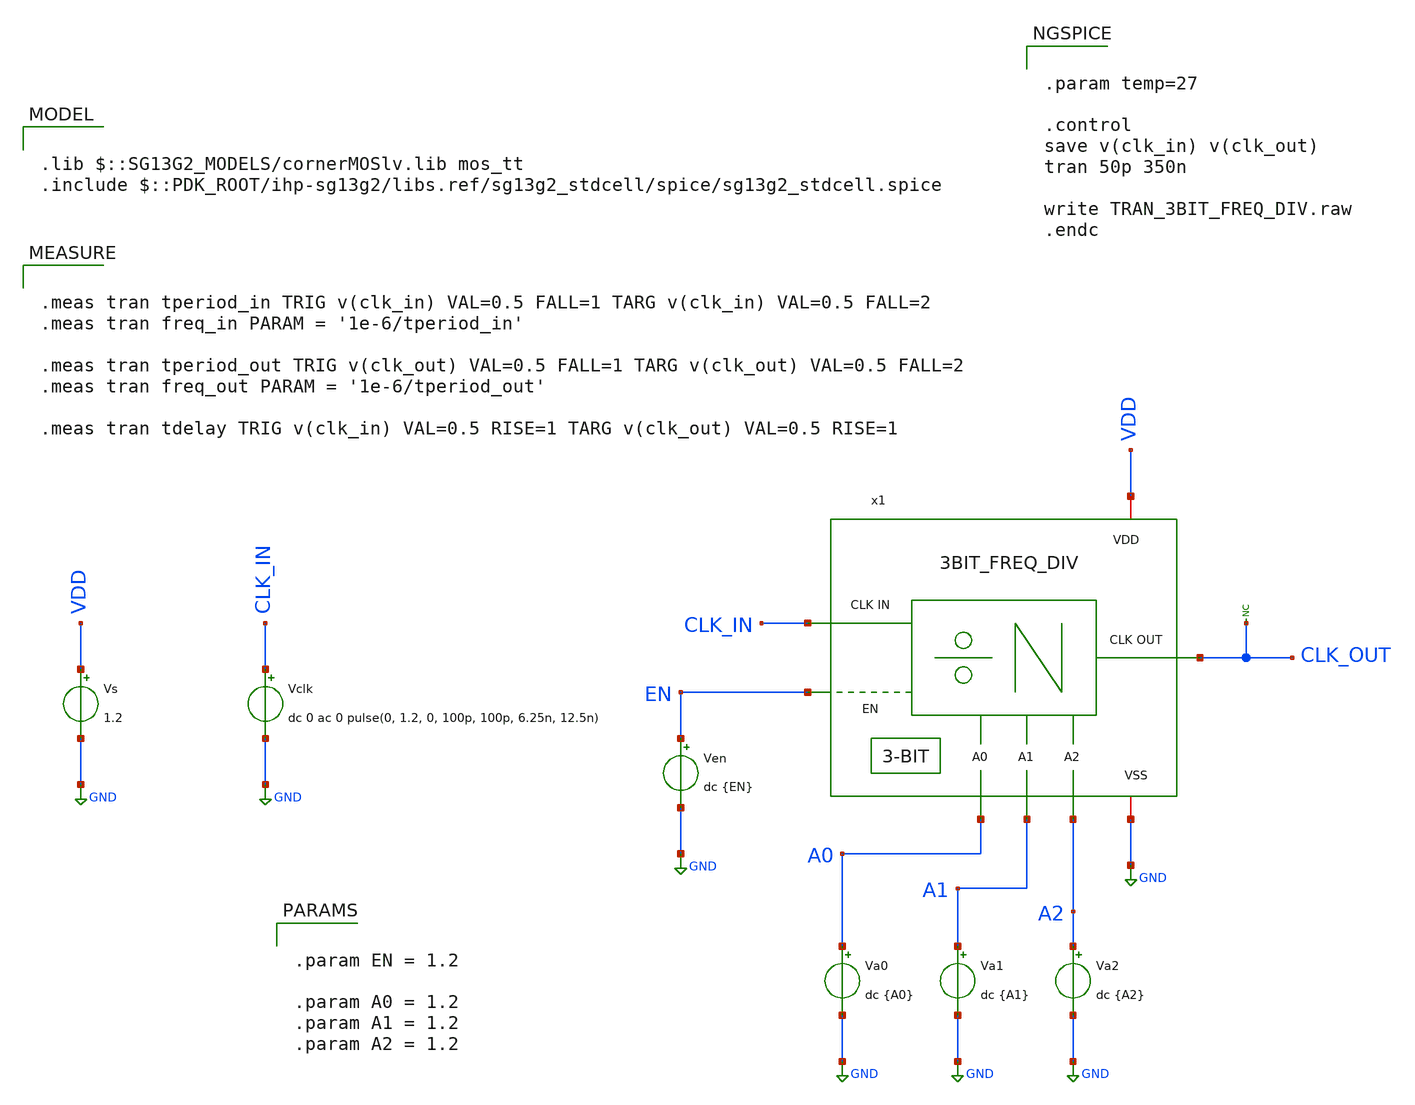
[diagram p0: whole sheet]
** sch_path: 30_MHz_Fractional_N_PLL/design_data/xschem/3BIT_FREQ_DIV_TB.sch
* IHP-GmbH/IHP-Open-PDK/ihp-sg13g2/libs.tech/xschem/sg13g2_stdcells/sg13g2_or3_1.sch:
* Copyright 2023 IHP PDK Authors
* Licensed under the Apache License, Version 2.0 (the "License");

.lib $::SG13G2_MODELS/cornerMOSlv.lib mos_tt
.include $::PDK_ROOT/ihp-sg13g2/libs.ref/sg13g2_stdcell/spice/sg13g2_stdcell.spice

**.subckt 3BIT_FREQ_DIV_TB
Vs VDD GND 1.2
Vclk CLK_IN GND dc 0 ac 0 pulse(0, 1.2, 0, 100p, 100p, 6.25n, 12.5n)
* noconn CLK_OUT
Ven EN GND dc {EN}
Va1 A1 GND dc {A1}
Va2 A2 GND dc {A2}
x1 A0 CLK_IN EN CLK_OUT A1 VDD GND A2 3BIT_FREQ_DIV
Va0 A0 GND dc {A0}
**** begin user architecture code


.meas tran tperiod_in TRIG v(clk_in) VAL=0.5 FALL=1 TARG v(clk_in) VAL=0.5 FALL=2
.meas tran freq_in PARAM = '1e-6/tperiod_in'

.meas tran tperiod_out TRIG v(clk_out) VAL=0.5 FALL=1 TARG v(clk_out) VAL=0.5 FALL=2
.meas tran freq_out PARAM = '1e-6/tperiod_out'

.meas tran tdelay TRIG v(clk_in) VAL=0.5 RISE=1 TARG v(clk_out) VAL=0.5 RISE=1




.param EN = 1.2

.param A0 = 1.2
.param A1 = 1.2
.param A2 = 1.2




.param temp=27

.control
save v(clk_in) v(clk_out)
tran 50p 350n

write TRAN_3BIT_FREQ_DIV.raw
.endc


**** end user architecture code
**.ends

* expanding   symbol:  3BIT_FREQ_DIV.sym # of pins=8
** sym_path: 30_MHz_Fractional_N_PLL/design_data/xschem/3BIT_FREQ_DIV.sym
** sch_path: 30_MHz_Fractional_N_PLL/design_data/xschem/3BIT_FREQ_DIV.sch
.subckt 3BIT_FREQ_DIV A0 CLK_IN EN CLK_OUT A1 VDD VSS A2
*.ipin CLK_IN
*.ipin EN
*.ipin A0
*.ipin A1
*.opin CLK_OUT
*.iopin VSS
*.iopin VDD
*.ipin A2
x1 VDD VSS nEQ0 net1 CLK net2 DIV_RST A0 FREQ_DIV_CELL
x2 VDD VSS nEQ1 net2 CLK net5 DIV_RST A1 FREQ_DIV_CELL
x3 net6 VDD VSS sg13g2_tiehi
x5 DIV_RST CLK_OUT net3 net3 net4 VDD VSS DFF_nCLK
x6 net7 VDD VSS sg13g2_tiehi
* noconn CLK_OUT
x7 CLK CLK_IN EN VDD VSS sg13g2_nand2_1
x4 DIV_RST nEQ2 nEQ1 nEQ0 VDD VSS sg13g2_or3_1
x8 VDD VSS nEQ2 net5 CLK Cout DIV_RST A2 FREQ_DIV_CELL
* noconn Cout
.ends


* expanding   symbol:  FREQ_DIV_CELL.sym # of pins=8
** sym_path: 30_MHz_Fractional_N_PLL/design_data/xschem/FREQ_DIV_CELL.sym
** sch_path: 30_MHz_Fractional_N_PLL/design_data/xschem/FREQ_DIV_CELL.sch
.subckt FREQ_DIV_CELL VDD VSS DIV Cin CLK Cout nRST BIT
*.ipin Cin
*.ipin CLK
*.ipin nRST
*.ipin BIT
*.opin DIV
*.opin Cout
*.iopin VSS
*.iopin VDD
x2 CLK net2 net1 net3 nRST VDD VSS DFF_nCLK
x3 DIV net2 BIT VDD VSS sg13g2_xor2_1
* noconn #net3
x1 net2 net1 Cin VDD VSS Cout HALF_ADD
.ends


* expanding   symbol:  DFF_nCLK.sym # of pins=7
** sym_path: 30_MHz_Fractional_N_PLL/design_data/xschem/DFF_nCLK.sym
** sch_path: 30_MHz_Fractional_N_PLL/design_data/xschem/DFF_nCLK.sch
.subckt DFF_nCLK nCLK Q D nQ nRST VDD VSS
*.ipin nCLK
*.ipin D
*.ipin nRST
*.opin Q
*.opin nQ
*.iopin VSS
*.iopin VDD
x1 Q nQ net1 D nRST VDD VSS sg13g2_dfrbp_1
x2 net1 nCLK VDD VSS sg13g2_inv_1
.ends


* expanding   symbol:  sg13g2_stdcells/sg13g2_nand2_1.sym # of pins=3
** sym_path: sg13g2_stdcells/sg13g2_nand2_1.sym
** sch_path: sg13g2_stdcells/sg13g2_nand2_1.sch
.subckt sg13g2_nand2_1 Y A B VDD VSS
*.iopin VDD
*.iopin VSS
*.ipin A
*.ipin B
*.opin Y
XM1 Y A net1 VSS sg13_lv_nmos w=740.00n l=130.00n ng=1 m=1 mm_ok=1
XM2 net1 B VSS VSS sg13_lv_nmos w=740.00n l=130.00n ng=1 m=1 mm_ok=1
XM3 Y A VDD VDD sg13_lv_pmos w=1.12u l=130.00n ng=1 m=1 mm_ok=1
XM4 Y B VDD VDD sg13_lv_pmos w=1.12u l=130.00n ng=1 m=1 mm_ok=1
.ends


* expanding   symbol:  sg13g2_stdcells/sg13g2_or3_1.sym # of pins=4
** sym_path: sg13g2_stdcells/sg13g2_or3_1.sym
** sch_path: sg13g2_stdcells/sg13g2_or3_1.sch
.subckt sg13g2_or3_1 X A B C VDD VSS
*.opin X
*.ipin C
*.ipin B
*.ipin A
*.iopin VDD
*.iopin VSS
XM1 net2 A VSS VSS sg13_lv_nmos w=550.00n l=130.00n ng=1 m=1 mm_ok=1
XM2 net2 B VSS VSS sg13_lv_nmos w=550.00n l=130.00n ng=1 m=1 mm_ok=1
XM3 net2 C VSS VSS sg13_lv_nmos w=550.00n l=130.00n ng=1 m=1 mm_ok=1
XM4 X net2 VSS VSS sg13_lv_nmos w=740.00n l=130.00n ng=1 m=1 mm_ok=1
XM5 net1 A VDD VDD sg13_lv_pmos w=1.000u l=130.00n ng=1 m=1 mm_ok=1
XM6 net3 B net1 VDD sg13_lv_pmos w=1.000u l=130.00n ng=1 m=1 mm_ok=1
XM7 net2 C net3 VDD sg13_lv_pmos w=1.000u l=130.00n ng=1 m=1 mm_ok=1
XM8 X net2 VDD VDD sg13_lv_pmos w=1.12u l=130.00n ng=1 m=1 mm_ok=1
.ends


* expanding   symbol:  sg13g2_stdcells/sg13g2_xor2_1.sym # of pins=3
** sym_path: sg13g2_stdcells/sg13g2_xor2_1.sym
** sch_path: sg13g2_stdcells/sg13g2_xor2_1.sch
.subckt sg13g2_xor2_1 X A B VDD VSS
*.opin X
*.ipin B
*.ipin A
*.iopin VDD
*.iopin VSS
XM1 net1 A VSS VSS sg13_lv_nmos w=550.00n l=130.00n ng=1 m=1 mm_ok=1
XM2 net1 B VSS VSS sg13_lv_nmos w=550.00n l=130.00n ng=1 m=1 mm_ok=1
XM3 X net1 VSS VSS sg13_lv_nmos w=740.00n l=130.00n ng=1 m=1 mm_ok=1
XM4 X B net3 VSS sg13_lv_nmos w=740.00n l=130.00n ng=1 m=1 mm_ok=1
XM5 net3 A VSS VSS sg13_lv_nmos w=740.00n l=130.00n ng=1 m=1 mm_ok=1
XM6 net4 A VDD VDD sg13_lv_pmos w=1.000u l=130.00n ng=1 m=1 mm_ok=1
XM7 net1 B net4 VDD sg13_lv_pmos w=1.000u l=130.00n ng=1 m=1 mm_ok=1
XM8 net2 A VDD VDD sg13_lv_pmos w=1.12u l=130.00n ng=1 m=1 mm_ok=1
XM9 X net1 net2 VDD sg13_lv_pmos w=1.12u l=130.00n ng=1 m=1 mm_ok=1
XM10 net2 B VDD VDD sg13_lv_pmos w=1.12u l=130.00n ng=1 m=1 mm_ok=1
.ends


* expanding   symbol:  HALF_ADD.sym # of pins=6
** sym_path: 30_MHz_Fractional_N_PLL/design_data/xschem/HALF_ADD.sym
** sch_path: 30_MHz_Fractional_N_PLL/design_data/xschem/HALF_ADD.sch
.subckt HALF_ADD inB sum inA VDD VSS cout
*.ipin inA
*.ipin inB
*.opin sum
*.opin cout
*.iopin VSS
*.iopin VDD
x1 sum inA inB VDD VSS sg13g2_xor2_1
x2 cout inA inB VDD VSS sg13g2_and2_1
.ends


* expanding   symbol:  sg13g2_stdcells/sg13g2_dfrbp_1.sym # of pins=5
** sym_path: sg13g2_stdcells/sg13g2_dfrbp_1.sym
** sch_path: sg13g2_stdcells/sg13g2_dfrbp_1.sch
.subckt sg13g2_dfrbp_1 Q Q_N CLK D RESET_B VDD VSS
*.ipin D
*.ipin RESET_B
*.ipin CLK
*.opin Q
*.opin Q_N
*.iopin VDD
*.iopin VSS
XM1 Db D net10 VSS sg13_lv_nmos w=420.00n l=130.00n ng=1 m=1 mm_ok=1
XM2 net10 RESET_B VSS VSS sg13_lv_nmos w=420.00n l=130.00n ng=1 m=1 mm_ok=1
XM3 net1 clkneg net9 VSS sg13_lv_nmos w=420.00n l=130.00n ng=1 m=1 mm_ok=1
XM4 net9 net1 VSS VSS sg13_lv_nmos w=420.00n l=130.00n ng=1 m=1 mm_ok=1
XM5 net1 net1 net5 VSS sg13_lv_nmos w=420.00n l=130.00n ng=1 m=1 mm_ok=1
XM6 net5 RESET_B VSS VSS sg13_lv_nmos w=420.00n l=130.00n ng=1 m=1 mm_ok=1
XM7 Q_N net1 VSS VSS sg13_lv_nmos w=740.00n l=130.00n ng=1 m=1 mm_ok=1
XM8 net2 net1 VSS VSS sg13_lv_nmos w=740.00n l=130.00n ng=1 m=1 mm_ok=1
XM9 Q net2 VSS VSS sg13_lv_nmos w=740.00n l=130.00n ng=1 m=1 mm_ok=1
XM10 clkneg CLK VSS VSS sg13_lv_nmos w=740.00n l=130.00n ng=1 m=1 mm_ok=1
XM11 clkpos clkneg VSS VSS sg13_lv_nmos w=740.00n l=130.00n ng=1 m=1 mm_ok=1
XM12 Db clkneg net3 VSS sg13_lv_nmos w=420.00n l=130.00n ng=1 m=1 mm_ok=1
XM13 net3 clkpos net8 VSS sg13_lv_nmos w=420.00n l=130.00n ng=1 m=1 mm_ok=1
XM14 net8 net3 net4 VSS sg13_lv_nmos w=420.00n l=130.00n ng=1 m=1 mm_ok=1
XM15 net4 RESET_B VSS VSS sg13_lv_nmos w=420.00n l=130.00n ng=1 m=1 mm_ok=1
XM16 net3 net3 VSS VSS sg13_lv_nmos w=740.00n l=130.00n ng=1 m=1 mm_ok=1
XM17 net3 clkpos net1 VSS sg13_lv_nmos w=740.00n l=130.00n ng=1 m=1 mm_ok=1
XM18 Db RESET_B VDD VDD sg13_lv_pmos w=420.00n l=130.00n ng=1 m=1 mm_ok=1
XM19 Db D VDD VDD sg13_lv_pmos w=420.00n l=130.00n ng=1 m=1 mm_ok=1
XM20 net7 net1 VDD VDD sg13_lv_pmos w=420.00n l=130.00n ng=1 m=1 mm_ok=1
XM21 net1 clkpos net7 VDD sg13_lv_pmos w=420.00n l=130.00n ng=1 m=1 mm_ok=1
XM22 net1 net1 VDD VDD sg13_lv_pmos w=420.00n l=130.00n ng=1 m=1 mm_ok=1
XM23 net1 RESET_B VDD VDD sg13_lv_pmos w=420.00n l=130.00n ng=1 m=1 mm_ok=1
XM24 Q_N net1 VDD VDD sg13_lv_pmos w=1.12u l=130.00n ng=1 m=1 mm_ok=1
XM25 net2 net1 VDD VDD sg13_lv_pmos w=1.12u l=130.00n ng=1 m=1 mm_ok=1
XM26 Q net2 VDD VDD sg13_lv_pmos w=1.12u l=130.00n ng=1 m=1 mm_ok=1
XM27 clkneg CLK VDD VDD sg13_lv_pmos w=1.12u l=130.00n ng=1 m=1 mm_ok=1
XM28 clkpos clkneg VDD VDD sg13_lv_pmos w=1.12u l=130.00n ng=1 m=1 mm_ok=1
XM29 Db clkpos net3 VDD sg13_lv_pmos w=420.00n l=130.00n ng=1 m=1 mm_ok=1
XM30 net6 net3 VDD VDD sg13_lv_pmos w=420.00n l=130.00n ng=1 m=1 mm_ok=1
XM31 net3 clkneg net6 VDD sg13_lv_pmos w=420.00n l=130.00n ng=1 m=1 mm_ok=1
XM32 net3 RESET_B VDD VDD sg13_lv_pmos w=420.00n l=130.00n ng=1 m=1 mm_ok=1
XM33 net3 net3 VDD VDD sg13_lv_pmos w=1.000u l=130.00n ng=1 m=1 mm_ok=1
XM34 net3 clkneg net1 VDD sg13_lv_pmos w=1.000u l=130.00n ng=1 m=1 mm_ok=1
.ends


* expanding   symbol:  sg13g2_stdcells/sg13g2_inv_1.sym # of pins=2
** sym_path: sg13g2_stdcells/sg13g2_inv_1.sym
** sch_path: sg13g2_stdcells/sg13g2_inv_1.sch
.subckt sg13g2_inv_1 Y A VDD VSS
*.opin Y
*.ipin A
*.iopin VDD
*.iopin VSS
XM1 Y A VSS VSS sg13_lv_nmos w=740.00n l=130.00n ng=1 m=1 mm_ok=1
XM2 Y A VDD VDD sg13_lv_pmos w=1.12u l=130.00n ng=1 m=1 mm_ok=1
.ends


* expanding   symbol:  sg13g2_stdcells/sg13g2_and2_1.sym # of pins=3
** sym_path: sg13g2_stdcells/sg13g2_and2_1.sym
** sch_path: sg13g2_stdcells/sg13g2_and2_1.sch
.subckt sg13g2_and2_1 X A B VDD VSS
*.ipin A
*.ipin B
*.opin X
*.iopin VDD
*.iopin VSS
XM1 net1 A net2 VSS sg13_lv_nmos w=640.00n l=130.00n ng=1 m=1 mm_ok=1
XM2 net2 B VSS VSS sg13_lv_nmos w=640.00n l=130.00n ng=1 m=1 mm_ok=1
XM3 X net1 VSS VSS sg13_lv_nmos w=740.00n l=130.00n ng=1 m=1 mm_ok=1
XM4 net1 B VDD VDD sg13_lv_pmos w=840.00n l=130.00n ng=1 m=1 mm_ok=1
XM5 net1 A VDD VDD sg13_lv_pmos w=840.00n l=130.00n ng=1 m=1 mm_ok=1
XM6 X net1 VDD VDD sg13_lv_pmos w=1.12u l=130.00n ng=1 m=1 mm_ok=1
.ends

.GLOBAL GND
.end
